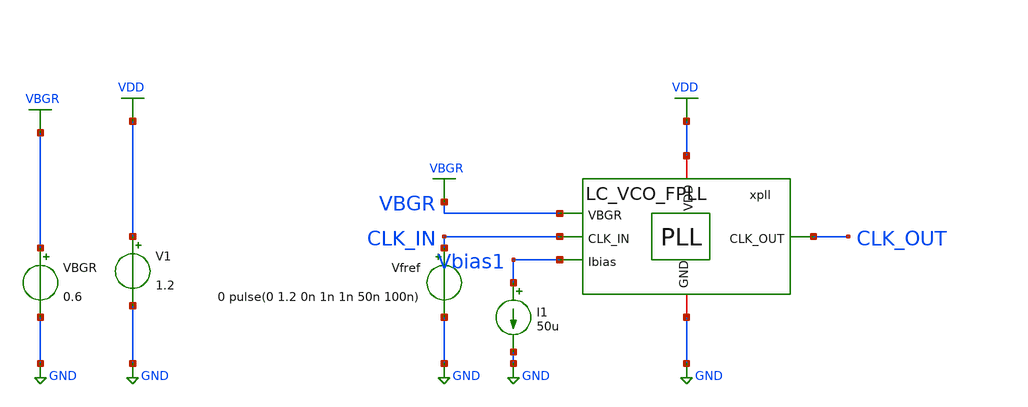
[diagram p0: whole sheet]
** sch_path: schematic/top-pll/LC_VCO_FPLL_tb.sch
**.subckt LC_VCO_FPLL_tb
V1 VDD GND 1.2
Vfref CLK_IN GND 0 pulse(0 1.2 0n 1n 1n 50n 100n)
I1 Vbias1 GND 50u
xpll VDD CLK_IN CLK_OUT VBGR Vbias1 GND LC_VCO_FPLL
VBGR VBGR GND 0.6
**** begin user architecture code



*****************************************************
* PLL + DSM Frequency Divider Testbench (Optimized)
*****************************************************

.option temp=27
.param VDD=1.2

* ==============================
* Include Models & Stimuli
* ==============================
.include ./IHP_4nH_Inductor.spice
.include stimuli_test.cir

* ==============================
* Simulation Options (Optimized for Speed & Stability)
* ==============================
* gear method improves stability for long oscillator runs
* reltol=1e-3 prevents the simulator from bogging down on microscopic errors
.options reltol=1e-3 abstol=1e-9 vntol=1e-6 method=gear

* ==============================
* Initial Conditions (Speed Hack)
* ==============================
* Uncomment the line below to pre-charge the loop filter to your expected
* V_tune voltage (e.g., 0.6V). This skips the massive initial frequency jump.

*.nodeset v(x1.vctrl)=0.606
*.nodeset v(x1.x1.ctrl1)=0.606
*.nodeset v(x1.x1.ctrl2)=0.606

.control
  * CRITICAL: Save ONLY essential low-frequency signals.
  * Saving 2.4GHz nodes for 100us will crash your memory.
  save xpll.vctrl xpll.up xpll.dn xpll.dsm_out clk_out clk_in vbias1 vbgr xpll.xcp.ctrl1
+ xpll.xcp.ctrl2 xpll.out xpll.sdata xpll.sclk xpll.en xpll.rst
  *save all


  * 20p defines the step to resolve the 2.4 GHz edges without forcing a maxstep.
  tran 10p 100u uic

  remzerovec
  write pll_sim_100u.raw
.endc






.lib cornerMOSlv.lib mos_tt
.lib cornerMOShv.lib mos_tt
.lib cornerHBT.lib hbt_typ
.lib cornerRES.lib res_typ
.lib cornerCAP.lib cap_typ_stat
.include /foss/pdks/ihp-sg13g2/libs.ref/sg13g2_stdcell/spice/sg13g2_stdcell.spice
.global VDD GND


.param CP_N_L = 1u
.param CP_N_W = 3u
.param CP_P_M = 1
.param CP_P_L = 1u
.param CP_P_W = 10u
.param CP_N_M = 1



**** end user architecture code
**.ends
.GLOBAL GND
.GLOBAL VDD
.GLOBAL VBGR
.end
